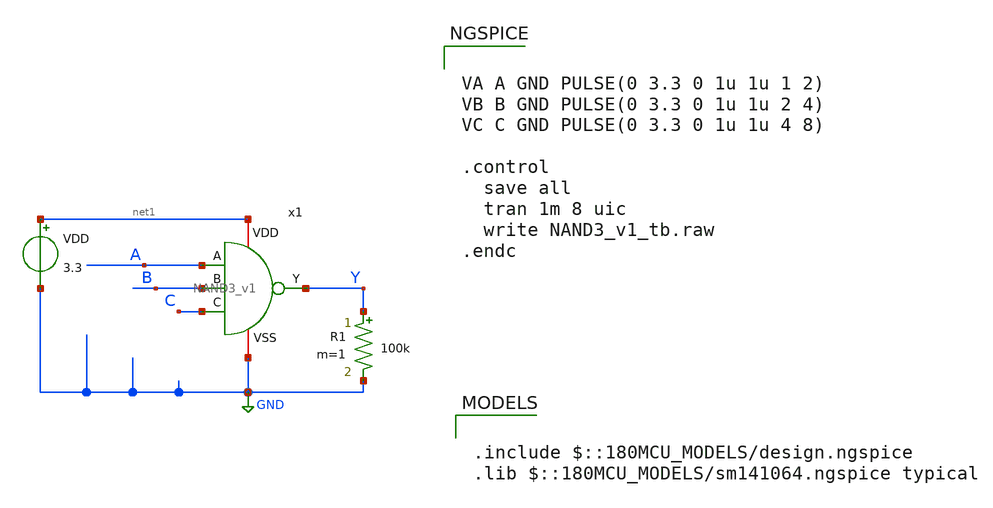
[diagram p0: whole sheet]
** sch_path: team_src/xschem/NAND3_v1_tb.sch
**.subckt NAND3_v1_tb
x1 C net1 Y A B GND NAND3_v1
VDD net1 GND 3.3
R1 Y GND 100k m=1
**** begin user architecture code

.include $::180MCU_MODELS/design.ngspice
.lib $::180MCU_MODELS/sm141064.ngspice typical



VA A GND PULSE(0 3.3 0 1u 1u 1 2)
VB B GND PULSE(0 3.3 0 1u 1u 2 4)
VC C GND PULSE(0 3.3 0 1u 1u 4 8)

.control
  save all
  tran 1m 8 uic
  write NAND3_v1_tb.raw
.endc


**** end user architecture code
**.ends

* expanding   symbol:  NAND3_v1.sym # of pins=6
** sym_path: team_src/xschem/NAND3_v1.sym
** sch_path: team_src/xschem/NAND3_v1.sch
.subckt NAND3_v1 C VDD Y A B VSS
*.iopin VSS
*.iopin VDD
*.ipin A
*.opin Y
*.ipin B
*.ipin C
XM1 net1 B net2 VSS nfet_03v3 L=0.28u W=3u nf=1 ad='int((nf+1)/2) * W/nf * 0.18u' as='int((nf+2)/2) * W/nf * 0.18u'
+ pd='2*int((nf+1)/2) * (W/nf + 0.18u)' ps='2*int((nf+2)/2) * (W/nf + 0.18u)' nrd='0.18u / W' nrs='0.18u / W'
+ sa=0 sb=0 sd=0 m=1
XM2 Y A net1 VSS nfet_03v3 L=0.28u W=3u nf=1 ad='int((nf+1)/2) * W/nf * 0.18u' as='int((nf+2)/2) * W/nf * 0.18u'
+ pd='2*int((nf+1)/2) * (W/nf + 0.18u)' ps='2*int((nf+2)/2) * (W/nf + 0.18u)' nrd='0.18u / W' nrs='0.18u / W'
+ sa=0 sb=0 sd=0 m=1
XM3 Y B VDD VDD pfet_03v3 L=0.28u W=1u nf=1 ad='int((nf+1)/2) * W/nf * 0.18u' as='int((nf+2)/2) * W/nf * 0.18u'
+ pd='2*int((nf+1)/2) * (W/nf + 0.18u)' ps='2*int((nf+2)/2) * (W/nf + 0.18u)' nrd='0.18u / W' nrs='0.18u / W'
+ sa=0 sb=0 sd=0 m=1
XM4 Y A VDD VDD pfet_03v3 L=0.28u W=1u nf=1 ad='int((nf+1)/2) * W/nf * 0.18u' as='int((nf+2)/2) * W/nf * 0.18u'
+ pd='2*int((nf+1)/2) * (W/nf + 0.18u)' ps='2*int((nf+2)/2) * (W/nf + 0.18u)' nrd='0.18u / W' nrs='0.18u / W'
+ sa=0 sb=0 sd=0 m=1
XM5 Y C VDD VDD pfet_03v3 L=0.28u W=1u nf=1 ad='int((nf+1)/2) * W/nf * 0.18u' as='int((nf+2)/2) * W/nf * 0.18u'
+ pd='2*int((nf+1)/2) * (W/nf + 0.18u)' ps='2*int((nf+2)/2) * (W/nf + 0.18u)' nrd='0.18u / W' nrs='0.18u / W'
+ sa=0 sb=0 sd=0 m=1
XM6 net2 C VSS VSS nfet_03v3 L=0.28u W=3u nf=1 ad='int((nf+1)/2) * W/nf * 0.18u' as='int((nf+2)/2) * W/nf * 0.18u'
+ pd='2*int((nf+1)/2) * (W/nf + 0.18u)' ps='2*int((nf+2)/2) * (W/nf + 0.18u)' nrd='0.18u / W' nrs='0.18u / W'
+ sa=0 sb=0 sd=0 m=1
.ends

.GLOBAL GND
.end
